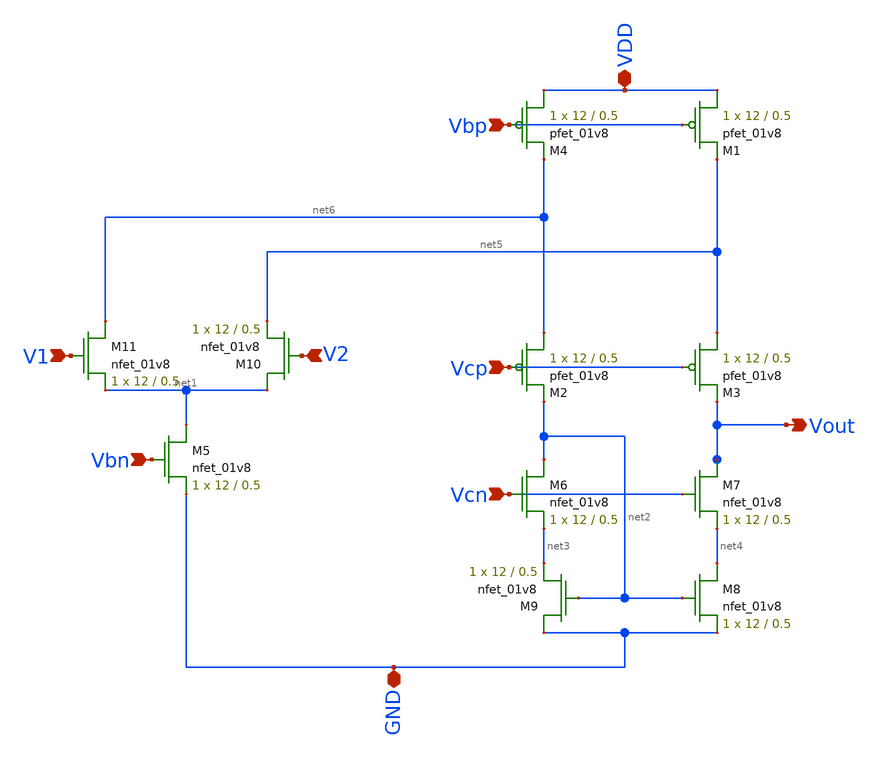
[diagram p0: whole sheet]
** sch_path: Miniproject3/layout&schematics/simple.sch
**.subckt simple Vbp VDD Vcp Vout V1 V2 Vbn GND Vcn
*.ipin Vbp
*.iopin VDD
*.ipin Vcp
*.opin Vout
*.ipin V1
*.ipin V2
*.ipin Vbn
*.iopin GND
*.ipin Vcn
XM1 VDD Vbp net5 VDD sky130_fd_pr__pfet_01v8 L=0.5 W=12 nf=1 ad='int((nf+1)/2) * W/nf * 0.29' as='int((nf+2)/2) * W/nf * 0.29'
+ pd='2*int((nf+1)/2) * (W/nf + 0.29)' ps='2*int((nf+2)/2) * (W/nf + 0.29)' nrd='0.29 / W' nrs='0.29 / W'
+ sa=0 sb=0 sd=0 mult=1 m=1
XM2 net6 Vcp net2 VDD sky130_fd_pr__pfet_01v8 L=0.5 W=12 nf=1 ad='int((nf+1)/2) * W/nf * 0.29' as='int((nf+2)/2) * W/nf * 0.29'
+ pd='2*int((nf+1)/2) * (W/nf + 0.29)' ps='2*int((nf+2)/2) * (W/nf + 0.29)' nrd='0.29 / W' nrs='0.29 / W'
+ sa=0 sb=0 sd=0 mult=1 m=1
XM3 net5 Vcp Vout VDD sky130_fd_pr__pfet_01v8 L=0.5 W=12 nf=1 ad='int((nf+1)/2) * W/nf * 0.29' as='int((nf+2)/2) * W/nf * 0.29'
+ pd='2*int((nf+1)/2) * (W/nf + 0.29)' ps='2*int((nf+2)/2) * (W/nf + 0.29)' nrd='0.29 / W' nrs='0.29 / W'
+ sa=0 sb=0 sd=0 mult=1 m=1
XM4 VDD Vbp net6 VDD sky130_fd_pr__pfet_01v8 L=0.5 W=12 nf=1 ad='int((nf+1)/2) * W/nf * 0.29' as='int((nf+2)/2) * W/nf * 0.29'
+ pd='2*int((nf+1)/2) * (W/nf + 0.29)' ps='2*int((nf+2)/2) * (W/nf + 0.29)' nrd='0.29 / W' nrs='0.29 / W'
+ sa=0 sb=0 sd=0 mult=1 m=1
XM5 net1 Vbn GND GND sky130_fd_pr__nfet_01v8 L=0.5 W=12 nf=1 ad='int((nf+1)/2) * W/nf * 0.29' as='int((nf+2)/2) * W/nf * 0.29'
+ pd='2*int((nf+1)/2) * (W/nf + 0.29)' ps='2*int((nf+2)/2) * (W/nf + 0.29)' nrd='0.29 / W' nrs='0.29 / W'
+ sa=0 sb=0 sd=0 mult=1 m=1
XM6 net2 Vcn net3 GND sky130_fd_pr__nfet_01v8 L=0.5 W=12 nf=1 ad='int((nf+1)/2) * W/nf * 0.29' as='int((nf+2)/2) * W/nf * 0.29'
+ pd='2*int((nf+1)/2) * (W/nf + 0.29)' ps='2*int((nf+2)/2) * (W/nf + 0.29)' nrd='0.29 / W' nrs='0.29 / W'
+ sa=0 sb=0 sd=0 mult=1 m=1
XM7 Vout Vcn net4 GND sky130_fd_pr__nfet_01v8 L=0.5 W=12 nf=1 ad='int((nf+1)/2) * W/nf * 0.29' as='int((nf+2)/2) * W/nf * 0.29'
+ pd='2*int((nf+1)/2) * (W/nf + 0.29)' ps='2*int((nf+2)/2) * (W/nf + 0.29)' nrd='0.29 / W' nrs='0.29 / W'
+ sa=0 sb=0 sd=0 mult=1 m=1
XM8 net4 net2 GND GND sky130_fd_pr__nfet_01v8 L=0.5 W=12 nf=1 ad='int((nf+1)/2) * W/nf * 0.29' as='int((nf+2)/2) * W/nf * 0.29'
+ pd='2*int((nf+1)/2) * (W/nf + 0.29)' ps='2*int((nf+2)/2) * (W/nf + 0.29)' nrd='0.29 / W' nrs='0.29 / W'
+ sa=0 sb=0 sd=0 mult=1 m=1
XM9 GND net2 net3 GND sky130_fd_pr__nfet_01v8 L=0.5 W=12 nf=1 ad='int((nf+1)/2) * W/nf * 0.29' as='int((nf+2)/2) * W/nf * 0.29'
+ pd='2*int((nf+1)/2) * (W/nf + 0.29)' ps='2*int((nf+2)/2) * (W/nf + 0.29)' nrd='0.29 / W' nrs='0.29 / W'
+ sa=0 sb=0 sd=0 mult=1 m=1
XM10 net1 V2 net5 GND sky130_fd_pr__nfet_01v8 L=0.5 W=12 nf=1 ad='int((nf+1)/2) * W/nf * 0.29' as='int((nf+2)/2) * W/nf * 0.29'
+ pd='2*int((nf+1)/2) * (W/nf + 0.29)' ps='2*int((nf+2)/2) * (W/nf + 0.29)' nrd='0.29 / W' nrs='0.29 / W'
+ sa=0 sb=0 sd=0 mult=1 m=1
XM11 net6 V1 net1 GND sky130_fd_pr__nfet_01v8 L=0.5 W=12 nf=1 ad='int((nf+1)/2) * W/nf * 0.29' as='int((nf+2)/2) * W/nf * 0.29'
+ pd='2*int((nf+1)/2) * (W/nf + 0.29)' ps='2*int((nf+2)/2) * (W/nf + 0.29)' nrd='0.29 / W' nrs='0.29 / W'
+ sa=0 sb=0 sd=0 mult=1 m=1
**.ends
.end
